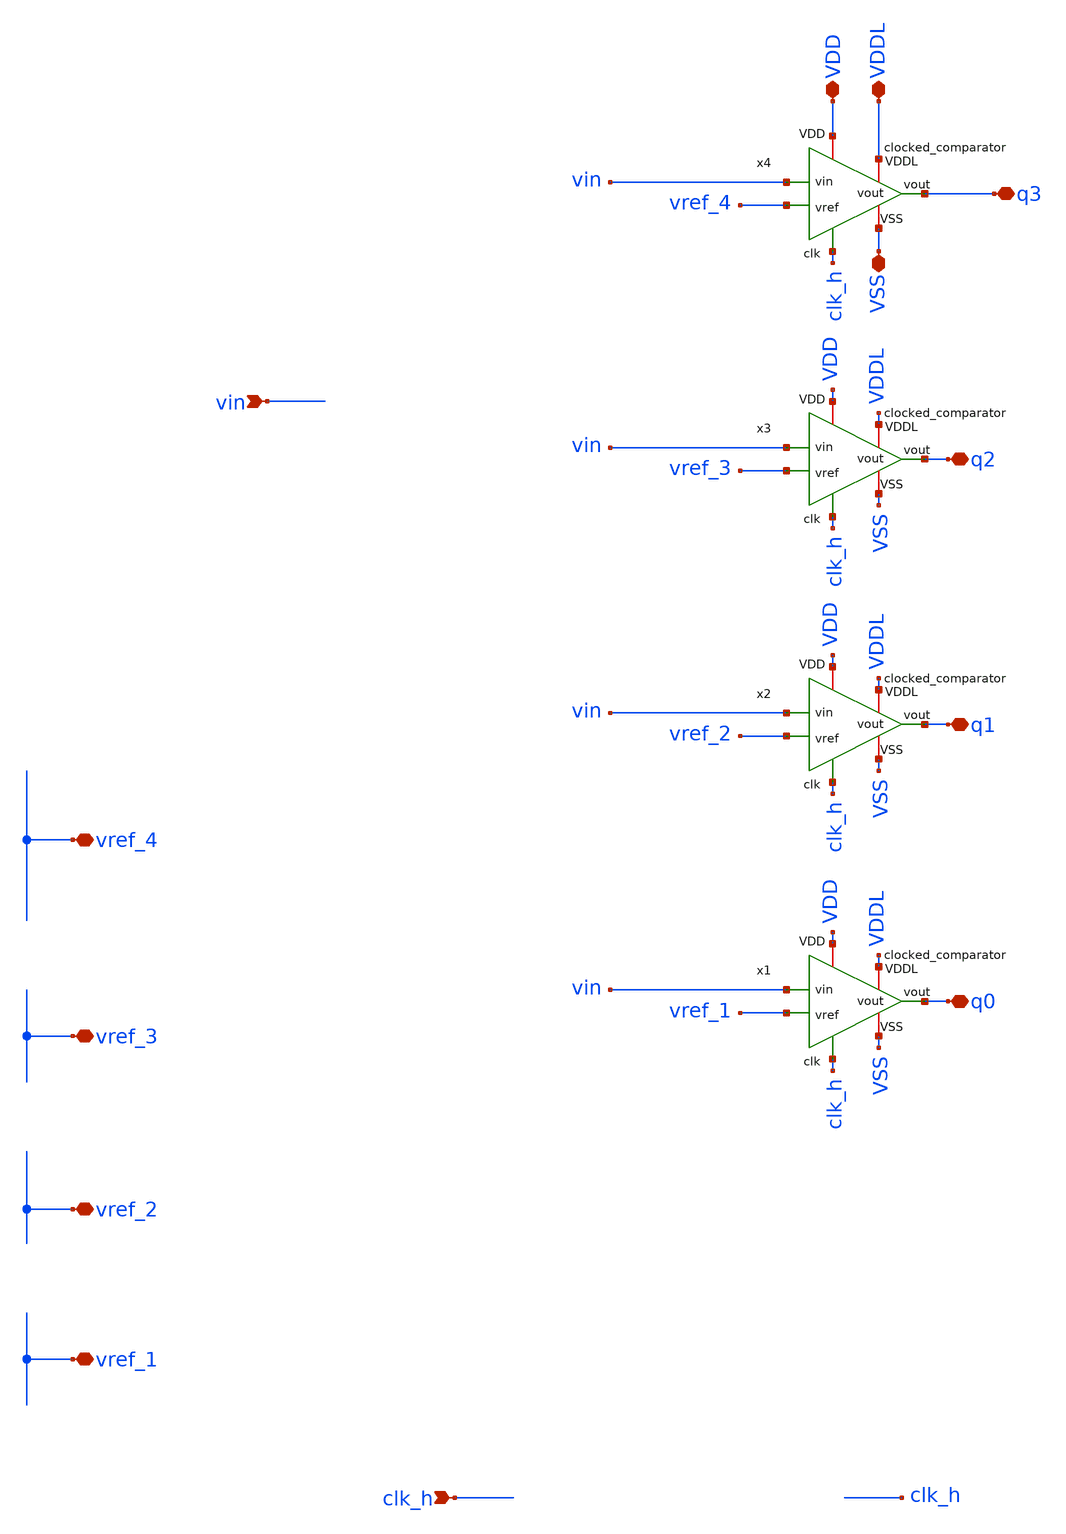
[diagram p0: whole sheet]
** sch_path: macros/heichips26_ook/macros/ook_analog_system/schematic/xschem/stash/comparator_group.sch
**.subckt comparator_group VDD VDDL q0 VSS clk_h q1 q2 q3 vin vref_4 vref_3 vref_2 vref_1
*.iopin VDD
*.iopin VDDL
*.iopin q0
*.iopin VSS
*.ipin clk_h
*.iopin q1
*.iopin q2
*.iopin q3
*.ipin vin
*.iopin vref_4
*.iopin vref_3
*.iopin vref_2
*.iopin vref_1
x1 clk_h vref_1 VDDL VDD vin q0 VSS clocked_comparator
x2 clk_h vref_2 VDDL VDD vin q1 VSS clocked_comparator
x3 clk_h vref_3 VDDL VDD vin q2 VSS clocked_comparator
x4 clk_h vref_4 VDDL VDD vin q3 VSS clocked_comparator
**.ends

* expanding   symbol:  clocked_comparator.sym # of pins=7
** sym_path: macros/heichips26_ook/macros/ook_analog_system/schematic/xschem/stash/clocked_comparator.sym
** sch_path: macros/heichips26_ook/macros/ook_analog_system/schematic/xschem/stash/clocked_comparator.sch
.subckt clocked_comparator clk vref VDDL VDD vin vout VSS
*.iopin VDD
*.iopin VDDL
*.ipin vin
*.ipin vref
*.iopin vout
*.ipin clk
*.iopin VSS
XMT VDD clkb net3 VDD sg13_hv_pmos w=5u l=0.5u ng=1 m=1 mm_ok=1
XM5 net3 vin net1 VDD sg13_hv_pmos w=5u l=0.5u ng=1 m=1 mm_ok=1
XM6 net1 net2 net5 VDD sg13_hv_pmos w=2u l=0.5u ng=1 m=1 mm_ok=1
XM7 net5 net2 VSS VSS sg13_hv_nmos w=1u l=0.5u ng=1 m=1 mm_ok=1
XM8 net3 vref net4 VDD sg13_hv_pmos w=5u l=0.5u ng=1 m=1 mm_ok=1
XM9 net4 net5 net2 VDD sg13_hv_pmos w=2u l=0.5u ng=1 m=1 mm_ok=1
XM10 net2 net5 VSS VSS sg13_hv_nmos w=1u l=0.5u ng=1 m=1 mm_ok=1
XM11 net5 clkb VSS VSS sg13_hv_nmos w=1u l=0.5u ng=1 m=1 mm_ok=1
XM12 net2 clkb VSS VSS sg13_hv_nmos w=1u l=0.5u ng=1 m=1 mm_ok=1
XM13 net4 clkb VSS VSS sg13_hv_nmos w=1u l=0.5u ng=1 m=1 mm_ok=1
XMPA1 VDDL net5 net8 VDDL sg13_hv_pmos w=4u l=0.5u ng=1 m=1 mm_ok=1
XMPA2 net8 net6 vout VDDL sg13_hv_pmos w=4u l=0.5u ng=1 m=1 mm_ok=1
XMNA1 vout net5 VSS VSS sg13_hv_nmos w=1u l=0.5u ng=1 m=1 mm_ok=1
XMNA2 vout net6 VSS VSS sg13_hv_nmos w=1u l=0.5u ng=1 m=1 mm_ok=1
XMPB1 VDDL net2 net7 VDDL sg13_hv_pmos w=4u l=0.5u ng=1 m=1 mm_ok=1
XMPB2 net7 vout net6 VDDL sg13_hv_pmos w=4u l=0.5u ng=1 m=1 mm_ok=1
XMNB1 net6 net2 VSS VSS sg13_hv_nmos w=1u l=0.5u ng=1 m=1 mm_ok=1
XMNB2 net6 vout VSS VSS sg13_hv_nmos w=1u l=0.5u ng=1 m=1 mm_ok=1
XM14 net1 clkb VSS VSS sg13_hv_nmos w=1u l=0.5u ng=1 m=1 mm_ok=1
XMIP1 clkb VSS clk VDD sg13_hv_pmos w=24u l=0.5u ng=12 m=1 mm_ok=1
XMIN1 clkb VDD clk VSS sg13_hv_nmos w=24u l=0.5u ng=12 m=1 mm_ok=1
XMT1 VDD VDD VDD VDD sg13_hv_pmos w=5u l=0.5u ng=1 m=1 mm_ok=1
XMT2 net3 net3 net3 VDD sg13_hv_pmos w=5u l=0.5u ng=1 m=1 mm_ok=1
XMIN2 clkb clkb clkb VSS sg13_hv_nmos w=2u l=0.5u ng=1 m=1 mm_ok=1
XMIN3 clk clk clk VSS sg13_hv_nmos w=2u l=0.5u ng=1 m=1 mm_ok=1
XMIP2 clk clk clk VDD sg13_hv_pmos w=2u l=0.5u ng=1 m=1 mm_ok=1
XMIP3 clkb clkb clkb VDD sg13_hv_pmos w=2u l=0.5u ng=1 m=1 mm_ok=1
XM1 net3 net3 net3 VDD sg13_hv_pmos w=5u l=0.5u ng=1 m=1 mm_ok=1
XM2 net3 net3 net3 VDD sg13_hv_pmos w=5u l=0.5u ng=1 m=1 mm_ok=1
XM3 net4 net4 net4 VDD sg13_hv_pmos w=5u l=0.5u ng=1 m=1 mm_ok=1
XM4 net1 net1 net1 VDD sg13_hv_pmos w=5u l=0.5u ng=1 m=1 mm_ok=1
XM15 net1 net1 net1 VDD sg13_hv_pmos w=2u l=0.5u ng=1 m=1 mm_ok=1
XM16 net4 net4 net4 VDD sg13_hv_pmos w=2u l=0.5u ng=1 m=1 mm_ok=1
XM17 net4 net4 net4 VSS sg13_hv_nmos w=1u l=0.5u ng=1 m=1 mm_ok=1
XM18 net1 net1 net1 VSS sg13_hv_nmos w=1u l=0.5u ng=1 m=1 mm_ok=1
XM19 net5 net5 net5 VDD sg13_hv_pmos w=2u l=0.5u ng=1 m=1 mm_ok=1
XM20 net2 net2 net2 VDD sg13_hv_pmos w=2u l=0.5u ng=1 m=1 mm_ok=1
XM21 VSS VSS VSS VSS sg13_hv_nmos w=1u l=0.5u ng=1 m=1 mm_ok=1
XM22 VSS VSS VSS VSS sg13_hv_nmos w=1u l=0.5u ng=1 m=1 mm_ok=1
XM23 net2 net2 net2 VSS sg13_hv_nmos w=1u l=0.5u ng=1 m=1 mm_ok=1
XM24 net5 net5 net5 VSS sg13_hv_nmos w=1u l=0.5u ng=1 m=1 mm_ok=1
XM25 VSS VSS VSS VSS sg13_hv_nmos w=1u l=0.5u ng=1 m=1 mm_ok=1
XM26 VSS VSS VSS VSS sg13_hv_nmos w=1u l=0.5u ng=1 m=1 mm_ok=1
XMPA3 VDDL VDDL VDDL VDDL sg13_hv_pmos w=4u l=0.5u ng=1 m=1 mm_ok=1
XMPB3 VDDL VDDL VDDL VDDL sg13_hv_pmos w=4u l=0.5u ng=1 m=1 mm_ok=1
XMPB4 net7 net7 net7 VDDL sg13_hv_pmos w=4u l=0.5u ng=1 m=1 mm_ok=1
XMPA4 net8 net8 net8 VDDL sg13_hv_pmos w=4u l=0.5u ng=1 m=1 mm_ok=1
XMPA5 net8 net8 net8 VDDL sg13_hv_pmos w=4u l=0.5u ng=1 m=1 mm_ok=1
XMPB5 net7 net7 net7 VDDL sg13_hv_pmos w=4u l=0.5u ng=1 m=1 mm_ok=1
XMPA6 vout vout vout VDDL sg13_hv_pmos w=4u l=0.5u ng=1 m=1 mm_ok=1
XMPB6 net6 net6 net6 VDDL sg13_hv_pmos w=4u l=0.5u ng=1 m=1 mm_ok=1
XMNA3 vout vout vout VSS sg13_hv_nmos w=1u l=0.5u ng=1 m=1 mm_ok=1
XMNA4 vout vout vout VSS sg13_hv_nmos w=1u l=0.5u ng=1 m=1 mm_ok=1
XMNB3 net6 net6 net6 VSS sg13_hv_nmos w=1u l=0.5u ng=1 m=1 mm_ok=1
XMNB4 net6 net6 net6 VSS sg13_hv_nmos w=1u l=0.5u ng=1 m=1 mm_ok=1
XMNB5 VSS VSS VSS VSS sg13_hv_nmos w=1u l=0.5u ng=1 m=1 mm_ok=1
XMNB6 VSS VSS VSS VSS sg13_hv_nmos w=1u l=0.5u ng=1 m=1 mm_ok=1
XMNA5 VSS VSS VSS VSS sg13_hv_nmos w=1u l=0.5u ng=1 m=1 mm_ok=1
XMNA6 VSS VSS VSS VSS sg13_hv_nmos w=1u l=0.5u ng=1 m=1 mm_ok=1
XM27 net5 net5 net5 VSS sg13_hv_nmos w=1u l=0.5u ng=1 m=1 mm_ok=1
XM28 VSS VSS VSS VSS sg13_hv_nmos w=1u l=0.5u ng=1 m=1 mm_ok=1
XM29 net2 net2 net2 VSS sg13_hv_nmos w=1u l=0.5u ng=1 m=1 mm_ok=1
XM30 VSS VSS VSS VSS sg13_hv_nmos w=1u l=0.5u ng=1 m=1 mm_ok=1
.ends

.end
